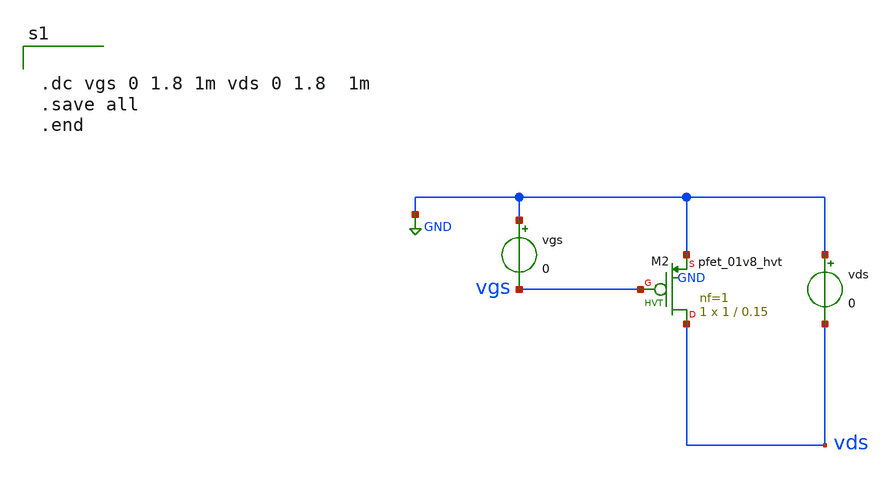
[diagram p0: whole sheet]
** sch_path: xschem/Polarizzazione.sch
**.subckt Polarizzazione
XM2 vds vgs GND GND sky130_fd_pr__pfet_01v8_hvt L=0.15 W=1 nf=1 ad='int((nf+1)/2) * W/nf * 0.29' as='int((nf+2)/2) * W/nf * 0.29'
+ pd='2*int((nf+1)/2) * (W/nf + 0.29)' ps='2*int((nf+2)/2) * (W/nf + 0.29)' nrd='0.29 / W' nrs='0.29 / W'
+ sa=0 sb=0 sd=0 mult=1 m=1
vgs GND vgs 0
vds GND vds 0
**** begin user architecture code


.dc vgs 0 1.8 1m vds 0 1.8  1m
.save all
.end


**** end user architecture code
**.ends
.GLOBAL GND
.end
